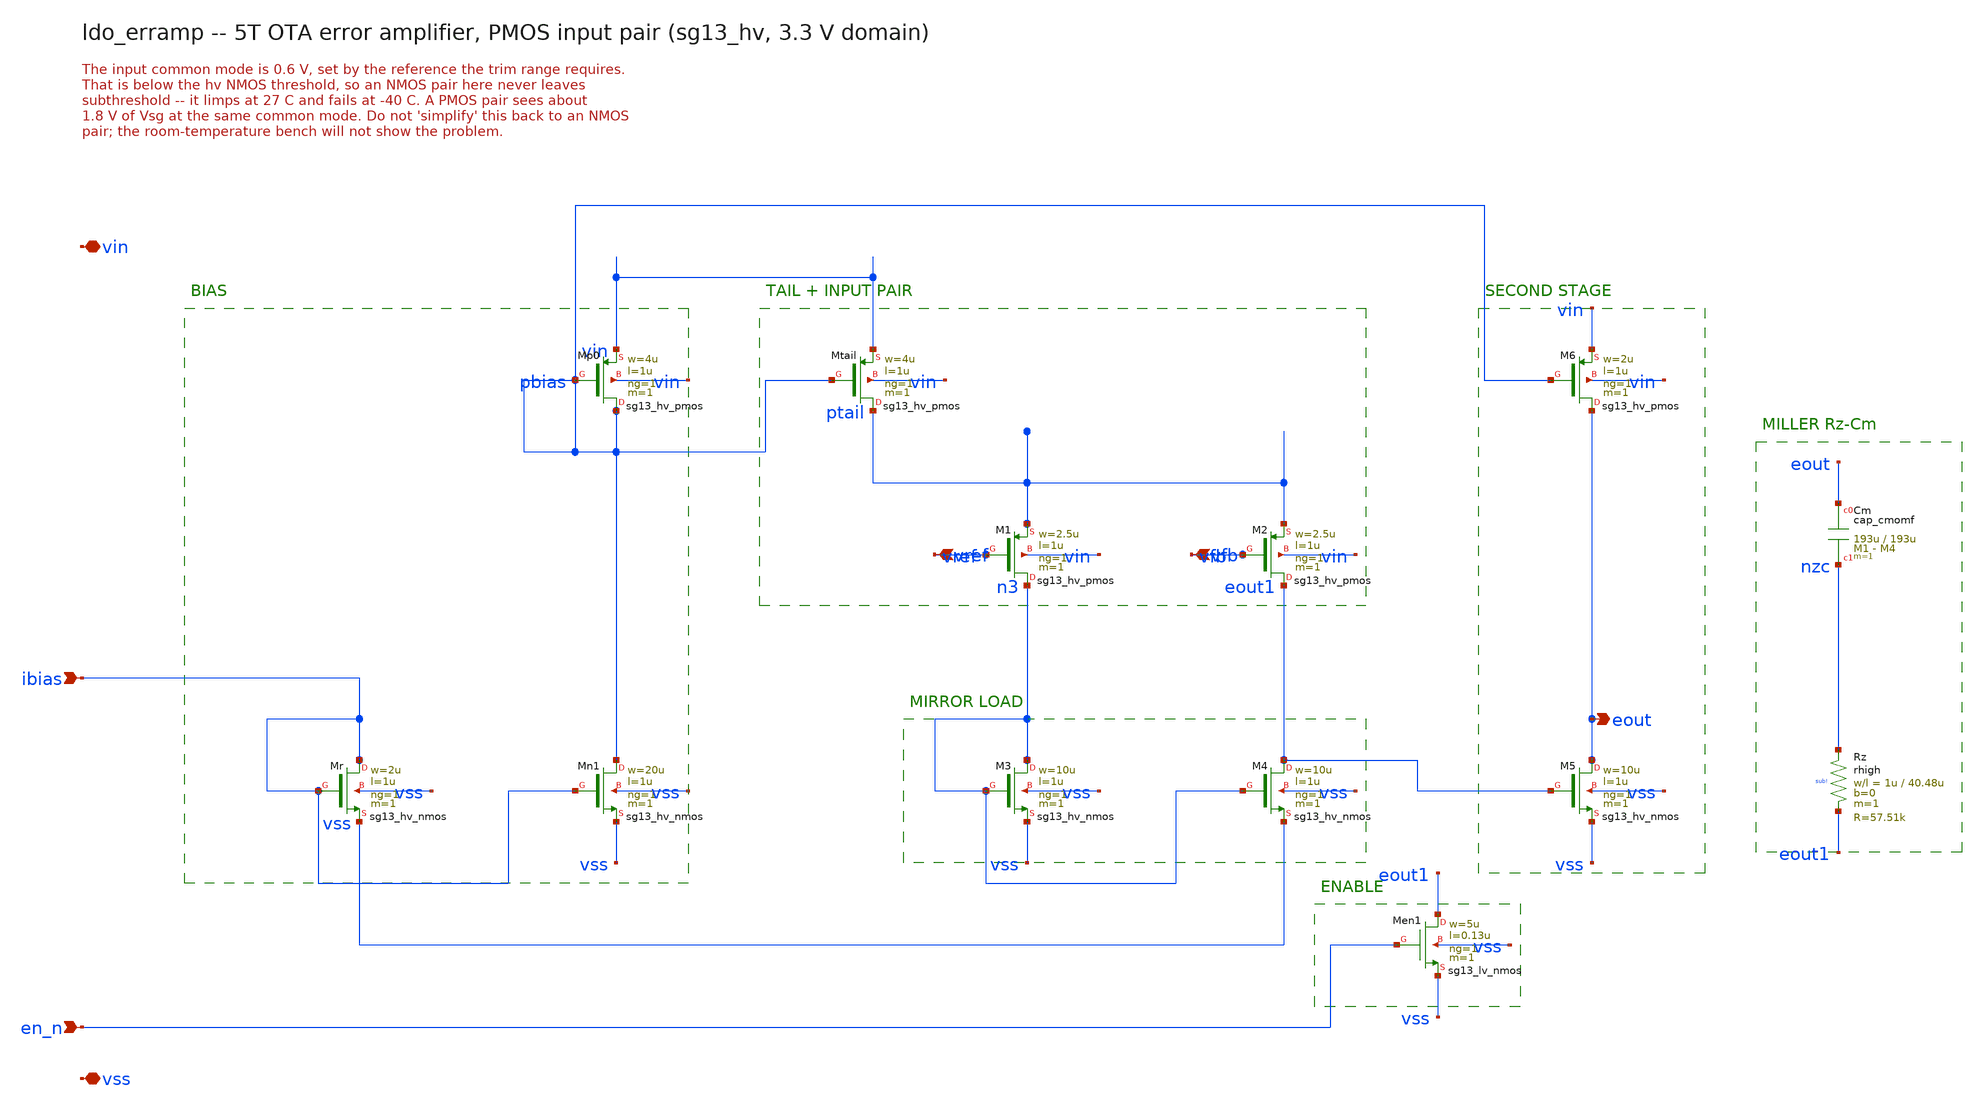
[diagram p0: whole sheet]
** sch_path: xschem/ldo_erramp.sch
**.subckt ldo_erramp vref vfb ibias en_n eout vin vss
*.ipin vref
*.ipin vfb
*.ipin ibias
*.ipin en_n
*.opin eout
*.iopin vin
*.iopin vss
XMp0 pbias pbias vin vin sg13_hv_pmos w=4u l=1u ng=1 m=1 mm_ok=1
XMtail ptail pbias vin vin sg13_hv_pmos w=4u l=1u ng=1 m=1 mm_ok=1
XM1 n3 vref ptail vin sg13_hv_pmos w=2.5u l=1u ng=1 m=1 mm_ok=1
XM2 eout1 vfb ptail vin sg13_hv_pmos w=2.5u l=1u ng=1 m=1 mm_ok=1
XM3 n3 n3 vss vss sg13_hv_nmos w=10u l=1u ng=1 m=1 mm_ok=1
XM4 eout1 n3 vss vss sg13_hv_nmos w=10u l=1u ng=1 m=1 mm_ok=1
XM5 eout eout1 vss vss sg13_hv_nmos w=10u l=1u ng=1 m=1 mm_ok=1
XM6 eout pbias vin vin sg13_hv_pmos w=2u l=1u ng=1 m=1 mm_ok=1
XCm eout nzc cap_cmomf w=193u l=193u mmin=1 mmax=4 subblock=0 rfmodel=0 subscale=1 m=1 mm_ok=1
XRz nzc eout1 sub! rhigh w=1u l=40.48u m=1 b=0 mm_ok=1
XMen1 eout1 en_n vss vss sg13_lv_nmos w=5u l=0.13u ng=1 m=1 mm_ok=1
XMn1 pbias ibias vss vss sg13_hv_nmos w=20u l=1u ng=1 m=1 mm_ok=1
XMr ibias ibias vss vss sg13_hv_nmos w=2u l=1u ng=1 m=1 mm_ok=1
**.ends
.end
